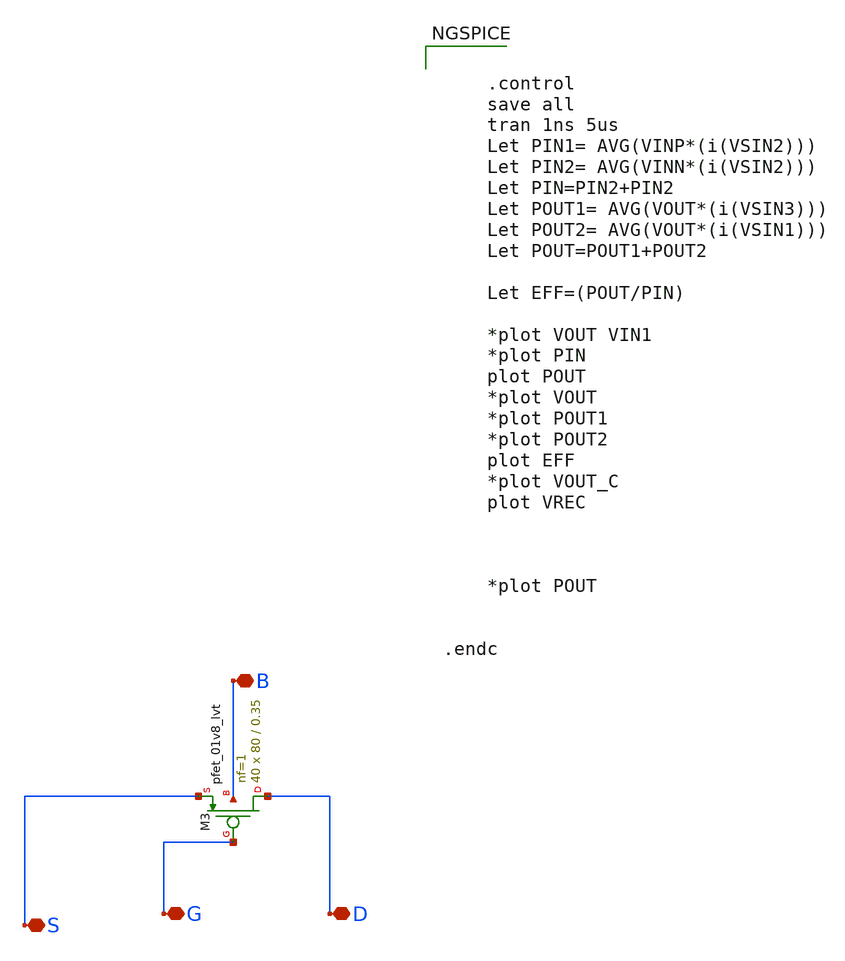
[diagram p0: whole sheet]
** sch_path: Schematics/PMOS_40.sch
**.subckt PMOS_40 D G S B
*.iopin D
*.iopin G
*.iopin S
*.iopin B
XM3 D G S B sky130_fd_pr__pfet_01v8_lvt L=0.35 W=80 nf=1 ad='int((nf+1)/2) * W/nf * 0.29' as='int((nf+2)/2) * W/nf * 0.29'
+ pd='2*int((nf+1)/2) * (W/nf + 0.29)' ps='2*int((nf+2)/2) * (W/nf + 0.29)' nrd='0.29 / W' nrs='0.29 / W'
+ sa=0 sb=0 sd=0 mult=40 m=40
**** begin user architecture code


	.control
	save all
	tran 1ns 5us
	Let PIN1= AVG(VINP*(i(VSIN2)))
	Let PIN2= AVG(VINN*(i(VSIN2)))
	Let PIN=PIN2+PIN2
	Let POUT1= AVG(VOUT*(i(VSIN3)))
	Let POUT2= AVG(VOUT*(i(VSIN1)))
	Let POUT=POUT1+POUT2

	Let EFF=(POUT/PIN)

	*plot VOUT VIN1
	*plot PIN
	plot POUT
	*plot VOUT
	*plot POUT1
	*plot POUT2
	plot EFF
	*plot VOUT_C
	plot VREC



	*plot POUT


.endc


 ** manual skywater pdks install (with patches applied)
* .lib $::SKYWATER_MODELS/models/sky130.lib.spice tt

** opencircuitdesign pdks install
.lib $::SKYWATER_MODELS/sky130.lib.spice tt

.param mc_mm_switch=0
.param mc_pr_switch=0

**** end user architecture code
**.ends
.end
